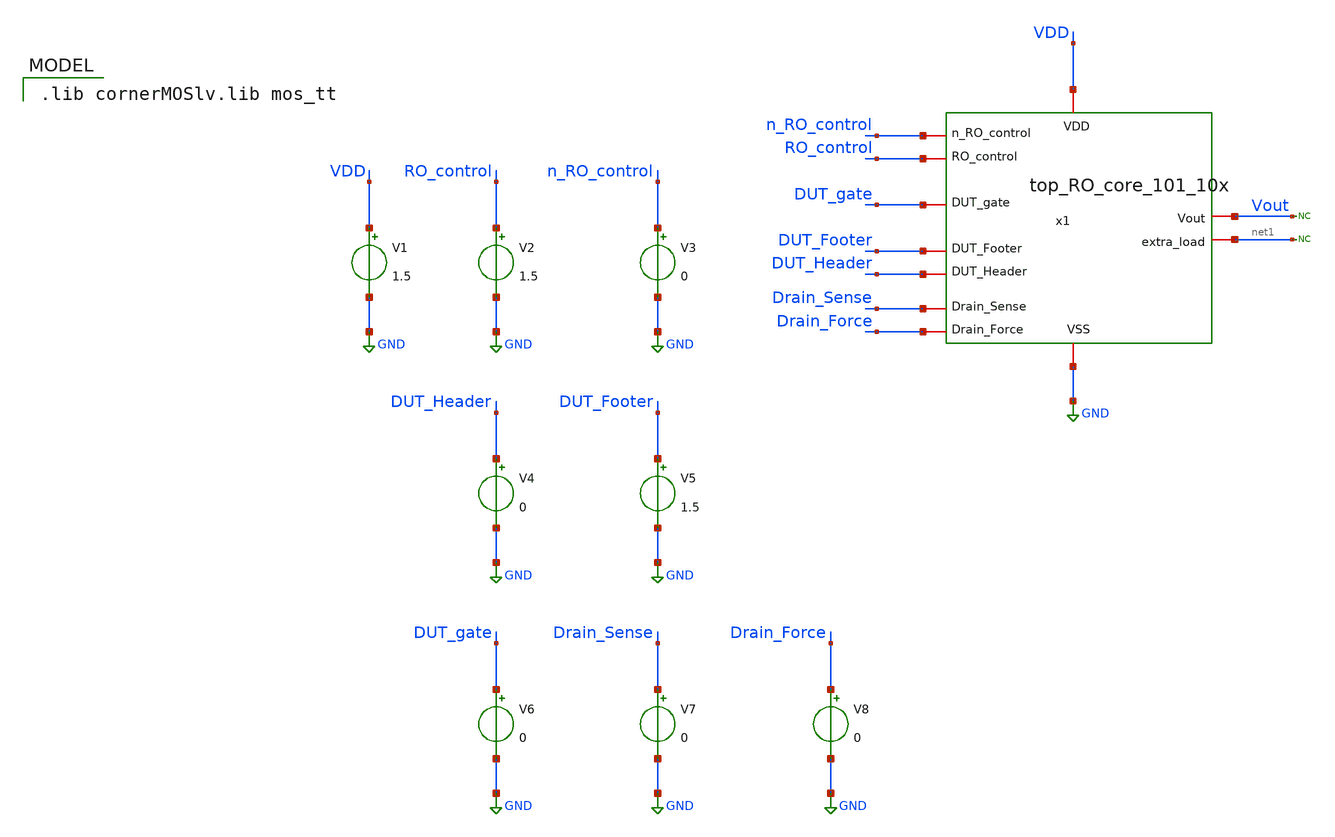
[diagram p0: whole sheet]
** sch_path: unic_cass_wrapper_user_project/ROs_reliability/top_RO_core_101_10x_tb.sch
**.subckt top_RO_core_101_10x_tb
V1 VDD GND 1.5
V2 RO_control GND 1.5
V3 n_RO_control GND 0
V4 DUT_Header GND 0
V5 DUT_Footer GND 1.5
* noconn #net1
* noconn Vout
V6 DUT_gate GND 0
V7 Drain_Sense GND 0
V8 Drain_Force GND 0
x1 VDD GND n_RO_control RO_control DUT_gate Vout DUT_Header DUT_Footer Drain_Force Drain_Sense net1
+ top_RO_core_101_10x
**** begin user architecture code


.ic V(x1.A[8])=0.8
.tran 0.1n 50n
.save all



 .lib cornerMOSlv.lib mos_tt

**** end user architecture code
**.ends

* expanding   symbol:  top_RO_core_101_10x.sym # of pins=11
** sym_path: top_RO_core_101_10x.sym
** sch_path: top_RO_core_101_10x.sch
.subckt top_RO_core_101_10x VDD VSS n_RO_control RO_control DUT_gate Vout DUT_Header DUT_Footer
+ Drain_Force Drain_Sense extra_load
*.iopin VDD
*.iopin VSS
*.iopin n_RO_control
*.iopin RO_control
*.iopin DUT_gate
*.iopin extra_load
*.iopin DUT_Header
*.iopin DUT_Footer
*.iopin Drain_Force
*.iopin Drain_Sense
*.iopin Vout
x4 VDD VSS A[97] A[96] rovcel2
x7 VDD VSS Vout A[100] rovcel2
x8[1] VDD VSS A[96] A[95] rovcel2
x8[2] VDD VSS A[95] A[94] rovcel2
x8[3] VDD VSS A[94] A[93] rovcel2
x8[4] VDD VSS A[93] A[92] rovcel2
x8[5] VDD VSS A[92] A[91] rovcel2
x8[6] VDD VSS A[91] A[90] rovcel2
x8[7] VDD VSS A[90] A[89] rovcel2
x8[8] VDD VSS A[89] A[88] rovcel2
x8[9] VDD VSS A[88] A[87] rovcel2
x8[10] VDD VSS A[87] A[86] rovcel2
x8[11] VDD VSS A[86] A[85] rovcel2
x8[12] VDD VSS A[85] A[84] rovcel2
x8[13] VDD VSS A[84] A[83] rovcel2
x8[14] VDD VSS A[83] A[82] rovcel2
x8[15] VDD VSS A[82] A[81] rovcel2
x8[16] VDD VSS A[81] A[80] rovcel2
x8[17] VDD VSS A[80] A[79] rovcel2
x8[18] VDD VSS A[79] A[78] rovcel2
x8[19] VDD VSS A[78] A[77] rovcel2
x8[20] VDD VSS A[77] A[76] rovcel2
x8[21] VDD VSS A[76] A[75] rovcel2
x8[22] VDD VSS A[75] A[74] rovcel2
x8[23] VDD VSS A[74] A[73] rovcel2
x8[24] VDD VSS A[73] A[72] rovcel2
x8[25] VDD VSS A[72] A[71] rovcel2
x8[26] VDD VSS A[71] A[70] rovcel2
x8[27] VDD VSS A[70] A[69] rovcel2
x8[28] VDD VSS A[69] A[68] rovcel2
x8[29] VDD VSS A[68] A[67] rovcel2
x8[30] VDD VSS A[67] A[66] rovcel2
x8[31] VDD VSS A[66] A[65] rovcel2
x8[32] VDD VSS A[65] A[64] rovcel2
x8[33] VDD VSS A[64] A[63] rovcel2
x8[34] VDD VSS A[63] A[62] rovcel2
x8[35] VDD VSS A[62] A[61] rovcel2
x8[36] VDD VSS A[61] A[60] rovcel2
x8[37] VDD VSS A[60] A[59] rovcel2
x8[38] VDD VSS A[59] A[58] rovcel2
x8[39] VDD VSS A[58] A[57] rovcel2
x8[40] VDD VSS A[57] A[56] rovcel2
x8[41] VDD VSS A[56] A[55] rovcel2
x8[42] VDD VSS A[55] A[54] rovcel2
x8[43] VDD VSS A[54] A[53] rovcel2
x8[44] VDD VSS A[53] A[52] rovcel2
x8[45] VDD VSS A[52] A[51] rovcel2
x8[46] VDD VSS A[51] A[50] rovcel2
x8[47] VDD VSS A[50] A[49] rovcel2
x8[48] VDD VSS A[49] A[48] rovcel2
x8[49] VDD VSS A[48] A[47] rovcel2
x8[50] VDD VSS A[47] A[46] rovcel2
x8[51] VDD VSS A[46] A[45] rovcel2
x8[52] VDD VSS A[45] A[44] rovcel2
x8[53] VDD VSS A[44] A[43] rovcel2
x8[54] VDD VSS A[43] A[42] rovcel2
x8[55] VDD VSS A[42] A[41] rovcel2
x8[56] VDD VSS A[41] A[40] rovcel2
x8[57] VDD VSS A[40] A[39] rovcel2
x8[58] VDD VSS A[39] A[38] rovcel2
x8[59] VDD VSS A[38] A[37] rovcel2
x8[60] VDD VSS A[37] A[36] rovcel2
x8[61] VDD VSS A[36] A[35] rovcel2
x8[62] VDD VSS A[35] A[34] rovcel2
x8[63] VDD VSS A[34] A[33] rovcel2
x8[64] VDD VSS A[33] A[32] rovcel2
x8[65] VDD VSS A[32] A[31] rovcel2
x8[66] VDD VSS A[31] A[30] rovcel2
x8[67] VDD VSS A[30] A[29] rovcel2
x8[68] VDD VSS A[29] A[28] rovcel2
x8[69] VDD VSS A[28] A[27] rovcel2
x8[70] VDD VSS A[27] A[26] rovcel2
x8[71] VDD VSS A[26] A[25] rovcel2
x8[72] VDD VSS A[25] A[24] rovcel2
x8[73] VDD VSS A[24] A[23] rovcel2
x8[74] VDD VSS A[23] A[22] rovcel2
x8[75] VDD VSS A[22] A[21] rovcel2
x8[76] VDD VSS A[21] A[20] rovcel2
x8[77] VDD VSS A[20] A[19] rovcel2
x8[78] VDD VSS A[19] A[18] rovcel2
x8[79] VDD VSS A[18] A[17] rovcel2
x8[80] VDD VSS A[17] A[16] rovcel2
x8[81] VDD VSS A[16] A[15] rovcel2
x8[82] VDD VSS A[15] A[14] rovcel2
x8[83] VDD VSS A[14] A[13] rovcel2
x8[84] VDD VSS A[13] A[12] rovcel2
x8[85] VDD VSS A[12] A[11] rovcel2
x8[86] VDD VSS A[11] A[10] rovcel2
x8[87] VDD VSS A[10] A[9] rovcel2
x8[88] VDD VSS A[9] A[8] rovcel2
x8[89] VDD VSS A[8] A[7] rovcel2
x8[90] VDD VSS A[7] A[6] rovcel2
x8[91] VDD VSS A[6] A[5] rovcel2
x8[92] VDD VSS A[5] A[4] rovcel2
x8[93] VDD VSS A[4] A[3] rovcel2
x8[94] VDD VSS A[3] A[2] rovcel2
x8[95] VDD VSS A[2] A[1] rovcel2
x8[96] VDD VSS A[1] Vout rovcel2
x3 DUT_Header DUT_Footer Drain_Force Drain_Sense RO_control n_RO_control VDD VSS A[98] extra_load
+ rovcel1_10
x1 VDD VSS A[97] n_RO_control A[98] RO_control DUT_gate rovcel3
x2 VDD VSS extra_load n_RO_control A[100] rovcel4
.ends


* expanding   symbol:  rovcel2.sym # of pins=4
** sym_path: rovcel2.sym
** sch_path: rovcel2.sch
.subckt rovcel2 VDD VSS Vout Vin
*.iopin VDD
*.iopin VSS
*.iopin Vin
*.iopin Vout
* noconn #net1
* noconn #net2
x5 VDD Vin Vout VSS inverter_RO_rel
x1 VDD VDD Vout net2 VSS VSS tgate
x3 VDD VDD Vout net1 VSS VSS tgate
.ends


* expanding   symbol:  rovcel1_10.sym # of pins=10
** sym_path: rovcel1_10.sym
** sch_path: rovcel1_10.sch
.subckt rovcel1_10 DUT_Header DUT_Footer Drain_Force Drain_Sense RO_control n_RO_control VDD VSS Vin
+ Vout
*.iopin VDD
*.iopin VSS
*.iopin Vin
*.iopin DUT_Header
*.iopin DUT_Footer
*.iopin Drain_Force
*.iopin Vout
*.iopin Drain_Sense
*.iopin RO_control
*.iopin n_RO_control
x1 VDD VSS Vin DUT_Header DUT_Footer Vout tristate_inv
x2 RO_control VDD Vout Drain_Sense VSS n_RO_control tgate
x3 RO_control VDD Vout Drain_Force VSS n_RO_control tgate_force10
.ends


* expanding   symbol:  rovcel3.sym # of pins=7
** sym_path: rovcel3.sym
** sch_path: rovcel3.sch
.subckt rovcel3 VDD VSS Vin n_RO_control Vout RO_control DUT_gate
*.iopin VDD
*.iopin VSS
*.iopin Vin
*.iopin n_RO_control
*.iopin RO_control
*.iopin DUT_gate
*.iopin Vout
* noconn #net1
x4 VDD VSS Vin n_RO_control RO_control Vout tristate_inv
x1 RO_control VDD Vout net1 VSS n_RO_control tgate
x5 RO_control VDD Vout DUT_gate VSS n_RO_control tgate
.ends


* expanding   symbol:  rovcel4.sym # of pins=5
** sym_path: rovcel4.sym
** sch_path: rovcel4.sch
.subckt rovcel4 VDD VSS Vin n_RO_control Vout
*.iopin VDD
*.iopin VSS
*.iopin Vin
*.iopin n_RO_control
*.iopin Vout
* noconn #net1
x4 n_RO_control VDD VSS Vin Vout inv1
x1 VDD VDD Vout VSS VSS VSS tgate
x5 VDD VDD Vout net1 VSS VSS tgate
.ends


* expanding   symbol:  inverter_RO_rel.sym # of pins=4
** sym_path: inverter_RO_rel.sym
** sch_path: inverter_RO_rel.sch
.subckt inverter_RO_rel VDD Vin Vout VSS
*.iopin VDD
*.iopin VSS
*.iopin Vin
*.iopin Vout
XM3 Vout Vin VDD VDD sg13_lv_pmos w=3.4u l=0.45u ng=1 m=4 mm_ok=1
XM1 VSS Vin Vout VSS sg13_lv_nmos w=1.3u l=0.45u ng=1 m=4 mm_ok=1
.ends


* expanding   symbol:  tgate.sym # of pins=6
** sym_path: tgate.sym
** sch_path: tgate.sch
.subckt tgate nclk VDD Vin Vout VSS clk
*.iopin nclk
*.iopin clk
*.iopin VDD
*.iopin VSS
*.iopin Vout
*.iopin Vin
XM3 Vout nclk Vin VDD sg13_lv_pmos w=3.4u l=0.45u ng=1 m=1 mm_ok=1
XM1 Vout clk Vin VSS sg13_lv_nmos w=1.3u l=0.45u ng=1 m=1 mm_ok=1
.ends


* expanding   symbol:  tristate_inv.sym # of pins=6
** sym_path: tristate_inv.sym
** sch_path: tristate_inv.sch
.subckt tristate_inv VDD VSS Vin Vup Vdn Vout
*.iopin VDD
*.iopin VSS
*.iopin Vin
*.iopin Vout
*.iopin Vup
*.iopin Vdn
XM5 Vout Vin net1 VDD sg13_lv_pmos w=3.4u l=0.45u ng=1 m=4 mm_ok=1
XM2 net2 Vin Vout VSS sg13_lv_nmos w=1.3u l=0.45u ng=1 m=4 mm_ok=1
XM1 net1 Vup VDD VDD sg13_lv_pmos w=3.4u l=0.45u ng=1 m=12 mm_ok=1
XM3 VSS Vdn net2 VSS sg13_lv_nmos w=1.3u l=0.45u ng=1 m=12 mm_ok=1
.ends


* expanding   symbol:  tgate_force10.sym # of pins=6
** sym_path: tgate_force10.sym
** sch_path: tgate_force10.sch
.subckt tgate_force10 nclk VDD Vin Vout VSS clk
*.iopin nclk
*.iopin clk
*.iopin VDD
*.iopin VSS
*.iopin Vout
*.iopin Vin
XM1 Vout nclk Vin VDD sg13_lv_pmos w=3.4u l=0.45u ng=1 m=12 mm_ok=1
XM3 Vout clk Vin VSS sg13_lv_nmos w=1.3u l=0.45u ng=1 m=12 mm_ok=1
.ends


* expanding   symbol:  inv1.sym # of pins=5
** sym_path: inv1.sym
** sch_path: inv1.sch
.subckt inv1 n_RO_control VDD VSS Vin Vout
*.iopin VDD
*.iopin VSS
*.iopin Vin
*.iopin Vout
*.iopin n_RO_control
XM1 net1 n_RO_control VDD VDD sg13_lv_pmos w=3.4u l=0.45u ng=1 m=12 mm_ok=1
XM5 Vout Vin net1 VDD sg13_lv_pmos w=3.4u l=0.45u ng=1 m=4 mm_ok=1
XM2 VSS Vin Vout VSS sg13_lv_nmos w=1.3u l=0.45u ng=1 m=4 mm_ok=1
.ends

.GLOBAL GND
.end
